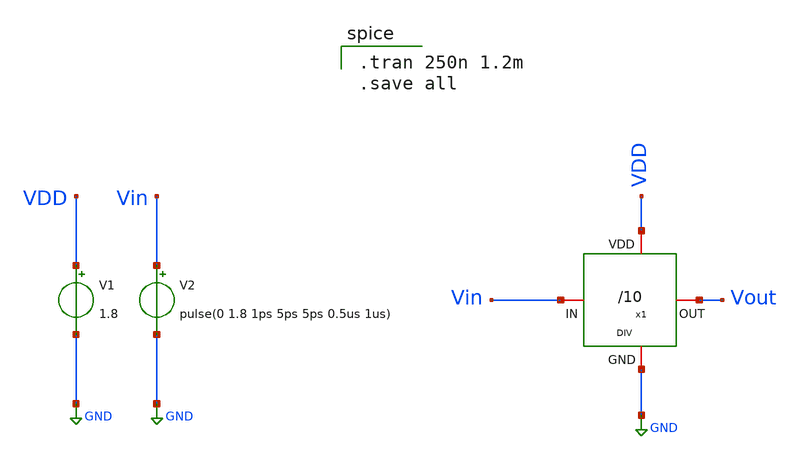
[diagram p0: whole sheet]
** sch_path: TB/DIV_TB.sch
**.subckt DIV_TB
V1 VDD GND 1.8
V2 Vin GND pulse(0 1.8 1ps 5ps 5ps 0.5us 1us)
x1 VDD Vout Vin GND DIV
**** begin user architecture code

.tran 250n 1.2m
.save all

 .lib $::SKYWATER_MODELS/sky130.lib.spice tt
.include $::SKYWATER_STDCELLS/sky130_fd_sc_hd.spice

**** end user architecture code
**.ends
.GLOBAL GND
.end
